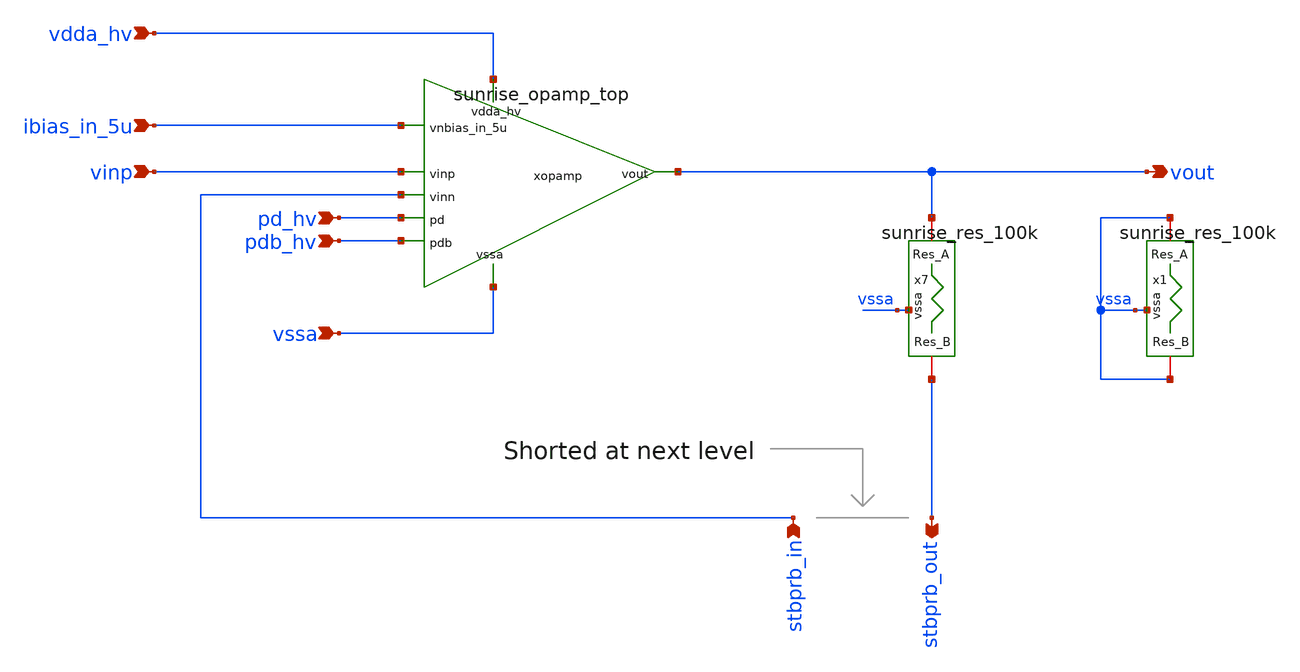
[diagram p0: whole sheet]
** sch_path: Schematics_Layout/sunrise_stg1_loop/sunrise_stg1_loop.sch
**.subckt sunrise_stg1_loop pd_hv pdb_hv ibias_in_5u vinp vdda_hv vssa vout stbprb_in stbprb_out
*.ipin pd_hv
*.ipin pdb_hv
*.ipin ibias_in_5u
*.ipin vinp
*.ipin vdda_hv
*.ipin vssa
*.opin vout
*.ipin stbprb_in
*.opin stbprb_out
x7 vssa stbprb_out vout sunrise_res_100k
xopamp vdda_hv ibias_in_5u vout vinp stbprb_in pd_hv pdb_hv vssa sunrise_opamp_top
x1 vssa vssa vssa sunrise_res_100k
**.ends
.end
